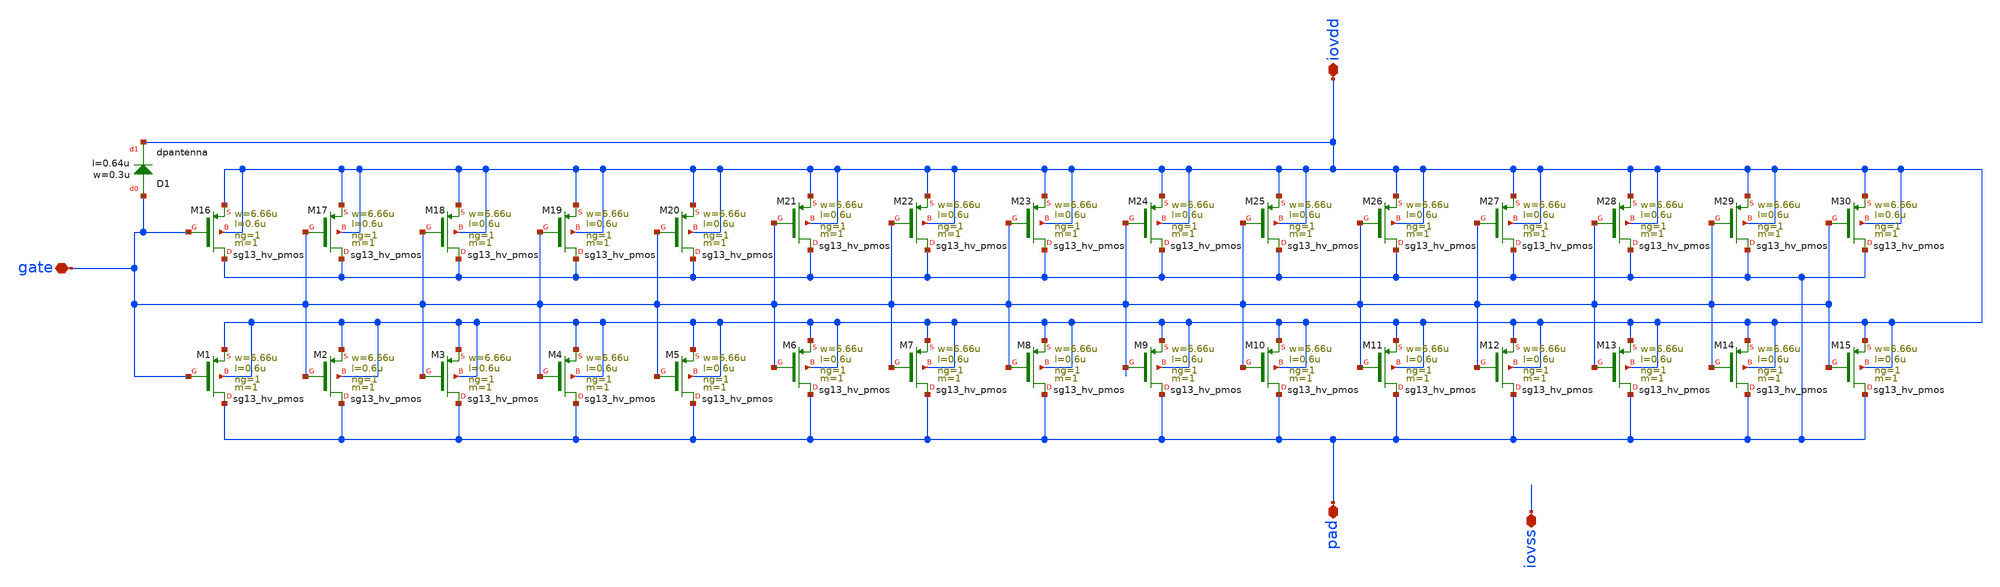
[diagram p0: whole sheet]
** sch_path: ihp-sg13g2/libs.ref/sg13g2_io/xschem/sg13g2_Clamp_P15N15D.sch
**.subckt sg13g2_Clamp_P15N15D pad gate iovdd iovss
*.iopin pad
*.iopin gate
*.iopin iovdd
*.iopin iovss
XM1 pad gate iovdd iovdd sg13_hv_pmos w=6.66u l=0.6u ng=1 m=1 mm_ok=1
XM2 pad gate iovdd iovdd sg13_hv_pmos w=6.66u l=0.6u ng=1 m=1 mm_ok=1
XM3 pad gate iovdd iovdd sg13_hv_pmos w=6.66u l=0.6u ng=1 m=1 mm_ok=1
XM4 pad gate iovdd iovdd sg13_hv_pmos w=6.66u l=0.6u ng=1 m=1 mm_ok=1
XM5 pad gate iovdd iovdd sg13_hv_pmos w=6.66u l=0.6u ng=1 m=1 mm_ok=1
XM6 pad gate iovdd iovdd sg13_hv_pmos w=6.66u l=0.6u ng=1 m=1 mm_ok=1
XM7 pad gate iovdd iovdd sg13_hv_pmos w=6.66u l=0.6u ng=1 m=1 mm_ok=1
XM8 pad gate iovdd iovdd sg13_hv_pmos w=6.66u l=0.6u ng=1 m=1 mm_ok=1
XM9 pad gate iovdd iovdd sg13_hv_pmos w=6.66u l=0.6u ng=1 m=1 mm_ok=1
XM10 pad gate iovdd iovdd sg13_hv_pmos w=6.66u l=0.6u ng=1 m=1 mm_ok=1
XM11 pad gate iovdd iovdd sg13_hv_pmos w=6.66u l=0.6u ng=1 m=1 mm_ok=1
XM12 pad gate iovdd iovdd sg13_hv_pmos w=6.66u l=0.6u ng=1 m=1 mm_ok=1
XM13 pad gate iovdd iovdd sg13_hv_pmos w=6.66u l=0.6u ng=1 m=1 mm_ok=1
XM14 pad gate iovdd iovdd sg13_hv_pmos w=6.66u l=0.6u ng=1 m=1 mm_ok=1
XM15 pad gate iovdd iovdd sg13_hv_pmos w=6.66u l=0.6u ng=1 m=1 mm_ok=1
XM16 pad gate iovdd iovdd sg13_hv_pmos w=6.66u l=0.6u ng=1 m=1 mm_ok=1
XM17 pad gate iovdd iovdd sg13_hv_pmos w=6.66u l=0.6u ng=1 m=1 mm_ok=1
XM18 pad gate iovdd iovdd sg13_hv_pmos w=6.66u l=0.6u ng=1 m=1 mm_ok=1
XM19 pad gate iovdd iovdd sg13_hv_pmos w=6.66u l=0.6u ng=1 m=1 mm_ok=1
XM20 pad gate iovdd iovdd sg13_hv_pmos w=6.66u l=0.6u ng=1 m=1 mm_ok=1
XM21 pad gate iovdd iovdd sg13_hv_pmos w=6.66u l=0.6u ng=1 m=1 mm_ok=1
XM22 pad gate iovdd iovdd sg13_hv_pmos w=6.66u l=0.6u ng=1 m=1 mm_ok=1
XM23 pad gate iovdd iovdd sg13_hv_pmos w=6.66u l=0.6u ng=1 m=1 mm_ok=1
XM24 pad gate iovdd iovdd sg13_hv_pmos w=6.66u l=0.6u ng=1 m=1 mm_ok=1
XM25 pad gate iovdd iovdd sg13_hv_pmos w=6.66u l=0.6u ng=1 m=1 mm_ok=1
XM26 pad gate iovdd iovdd sg13_hv_pmos w=6.66u l=0.6u ng=1 m=1 mm_ok=1
XM27 pad gate iovdd iovdd sg13_hv_pmos w=6.66u l=0.6u ng=1 m=1 mm_ok=1
XM28 pad gate iovdd iovdd sg13_hv_pmos w=6.66u l=0.6u ng=1 m=1 mm_ok=1
XM29 pad gate iovdd iovdd sg13_hv_pmos w=6.66u l=0.6u ng=1 m=1 mm_ok=1
XM30 pad gate iovdd iovdd sg13_hv_pmos w=6.66u l=0.6u ng=1 m=1 mm_ok=1
XD1 gate iovdd dpantenna l=0.64u w=0.3u
**.ends
.end
